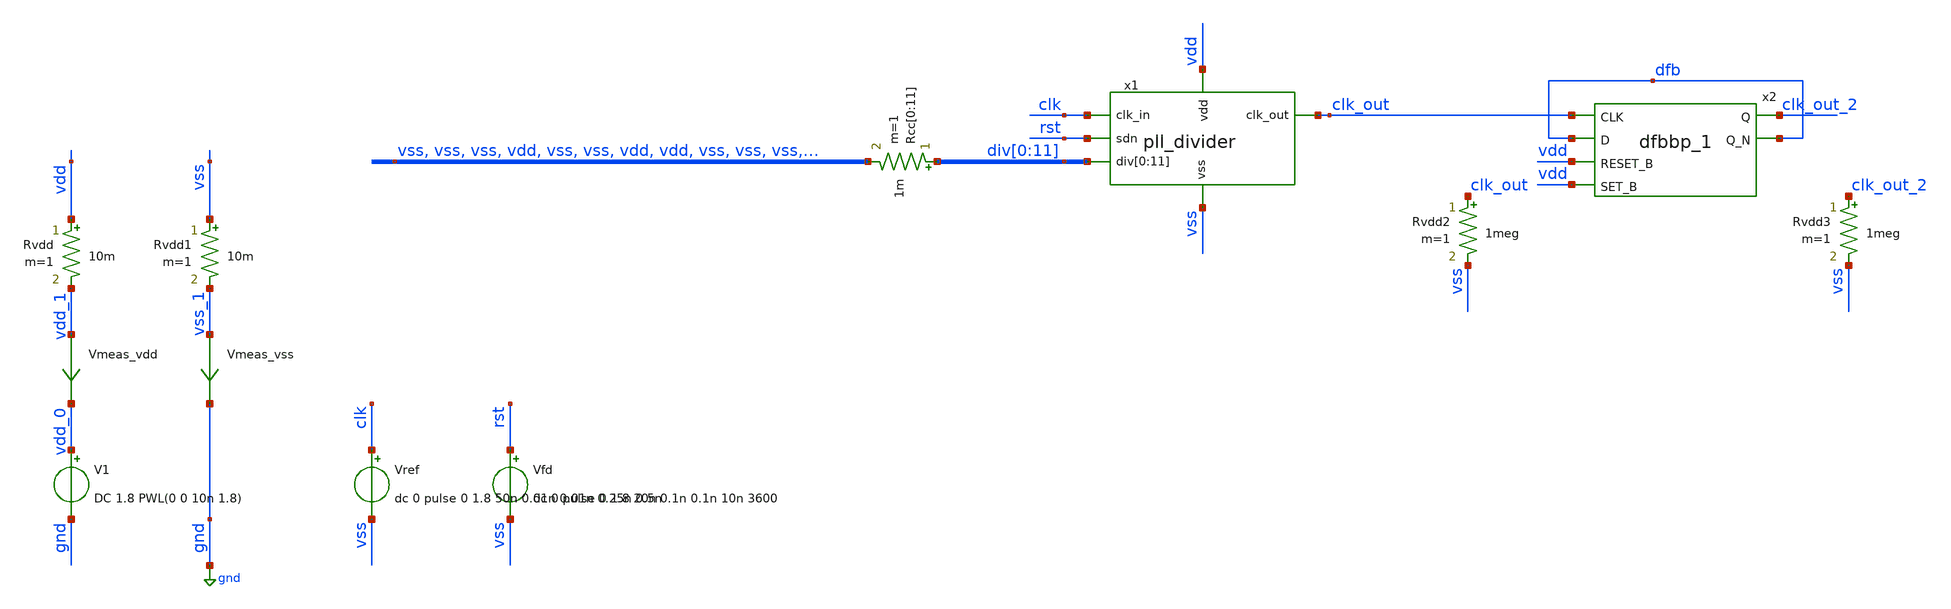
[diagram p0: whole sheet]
** sch_path: pll/pll_divider/simulation/pll_divider_tb.sch
**.subckt pll_divider_tb
V1 vdd_0 gnd DC 1.8 PWL(0 0 10n 1.8)
Vmeas_vdd vdd_1 vdd_0 0
.save i(vmeas_vdd)
Vref clk vss dc 0 pulse 0 1.8 50n 0.01n 0.01n 0.25n 0.5n
Vfd rst vss dc 0 pulse 0 1.8 20n 0.1n 0.1n 10n 3600
Vmeas_vss vss_1 gnd 0
.save i(vmeas_vss)
Rvdd vdd vdd_1 10m m=1
Rvdd1 vss vss_1 10m m=1
Rvdd2 clk_out vss 1meg m=1
Rcc[0] div[0] vss 1m m=1
Rcc[1] div[1] vss 1m m=1
Rcc[2] div[2] vss 1m m=1
Rcc[3] div[3] vdd 1m m=1
Rcc[4] div[4] vss 1m m=1
Rcc[5] div[5] vss 1m m=1
Rcc[6] div[6] vdd 1m m=1
Rcc[7] div[7] vdd 1m m=1
Rcc[8] div[8] vss 1m m=1
Rcc[9] div[9] vss 1m m=1
Rcc[10] div[10] vss 1m m=1
Rcc[11] div[11] vss 1m m=1
Rvdd3 clk_out_2 vss 1meg m=1
x2 clk_out dfb vdd vdd vss vss vdd vdd clk_out_2 dfb sky130_fd_sc_hd__dfbbp_1
x1 vdd vss clk_out clk rst div[0] div[1] div[2] div[3] div[4] div[5] div[6] div[7] div[8] div[9]
+ div[10] div[11] pll_divider
**** begin user architecture code



*.option savecurrents
*.option rshunt = 1e12
*.option gmin = 1e-24

** Settings for PSS osciallator
*.option reltol=1e-5
*.option vntol=3e-8
*.option abstol=1e-13
**.option chgtol=1e-12
*.option trtol=10
.option method=gear

.control

* #################################################################
* #
* #                         OPERATING POINT
* #
* #################################################################
reset
save all

op
set filetype=binary
write pll_divider_tb.raw all

* #################################################################
* #
* #                 TRANSIENT OSCILATION REGIME
* #
* #################################################################
reset
setplot const
*save all
save v(vdd) v(vdd_1) v(vss) v(vss_1)
save v(clk) v(clk_out) v(clk_out_2)
save v(x1.ps_out) v(x1.ps_out_b) v(x1.ps_mod)
save v('x1.q<0>') v('x1.q<1>') v('x1.q<2>') v('x1.q<3>') v('x1.q<4>') v('x1.q<5>') v('x1.q<6>') v('x1.q<7>')
+ v('x1.q<8>') v('x1.q<9>') v('x1.q<10>') v('x1.q<11>')
save v(x1.div_rst) v(x1.int_rst) v(x1.div_rst_b) v(x1.ps_out_b) v(x1.rst_0_2) v(x1.rst_3_11)

tran 0.05n 1u uic
set filetype=ascii
write pll_divider_tb_tran.raw v(clk) v(clk_out)

* Plot outputs
plot v(clk)+2 v(clk_out)+0 v(clk_out_2)-1
plot v(clk)+28 v(x1.ps_out)+26 v(x1.ps_mod)+24 v("x1.q<0>")+22 v("x1.q<1>")+20 v("x1.q<2>")+18
+ v("x1.q<3>")+16 v("x1.q<4>")+14 v("x1.q<5>")+12 v("x1.q<6>")+10 v("x1.q<7>")+8 v("x1.q<8>")+6 v("x1.q<9>")+4
+ v("x1.q<10>")+2 v("x1.q<11>")+0 v(x1.div_rst)-2 v(x1.int_rst)-4  v(x1.div_rst_b)-6 v(x1.rst_0_2)-8
+ v(x1.rst_3_11)-10 v(x1.ps_out_b)-12 v(clk_out)-14

*rusage
.endc



.options wnflag=1
.include $::SKYWATER_MODELS/cells/nfet_01v8/sky130_fd_pr__nfet_01v8__tt.corner.spice
.include $::SKYWATER_MODELS/cells/nfet_01v8_lvt/sky130_fd_pr__nfet_01v8_lvt__tt.corner.spice
.include $::SKYWATER_MODELS/cells/pfet_01v8/sky130_fd_pr__pfet_01v8__tt.corner.spice
.include $::SKYWATER_MODELS/cells/nfet_03v3_nvt/sky130_fd_pr__nfet_03v3_nvt__tt.corner.spice
.include $::SKYWATER_MODELS/cells/nfet_05v0_nvt/sky130_fd_pr__nfet_05v0_nvt__tt.corner.spice
.include $::SKYWATER_MODELS/cells/esd_nfet_01v8/sky130_fd_pr__esd_nfet_01v8__tt.corner.spice
.include $::SKYWATER_MODELS/cells/pfet_01v8_lvt/sky130_fd_pr__pfet_01v8_lvt__tt.corner.spice
.include $::SKYWATER_MODELS/cells/pfet_01v8_hvt/sky130_fd_pr__pfet_01v8_hvt__tt.corner.spice
.include $::SKYWATER_MODELS/cells/esd_pfet_g5v0d10v5/sky130_fd_pr__esd_pfet_g5v0d10v5__tt.corner.spice
.include $::SKYWATER_MODELS/cells/pfet_g5v0d10v5/sky130_fd_pr__pfet_g5v0d10v5__tt.corner.spice
.include $::SKYWATER_MODELS/cells/pfet_g5v0d16v0/sky130_fd_pr__pfet_g5v0d16v0__tt.corner.spice
.include $::SKYWATER_MODELS/cells/nfet_g5v0d10v5/sky130_fd_pr__nfet_g5v0d10v5__tt.corner.spice
.include $::SKYWATER_MODELS/cells/nfet_g5v0d16v0/sky130_fd_pr__nfet_g5v0d16v0__tt_discrete.corner.spice
.include $::SKYWATER_MODELS/cells/esd_nfet_g5v0d10v5/sky130_fd_pr__esd_nfet_g5v0d10v5__tt.corner.spice
.include $::SKYWATER_MODELS/models/corners/tt/nonfet.spice

.include $::SKYWATER_MODELS/cells/cap_var_hvt/sky130_fd_pr__cap_var_hvt.model.spice

* Mismatch parameters
.include $::SKYWATER_MODELS/cells/nfet_01v8/sky130_fd_pr__nfet_01v8__mismatch.corner.spice
.include $::SKYWATER_MODELS/cells/pfet_01v8/sky130_fd_pr__pfet_01v8__mismatch.corner.spice
.include $::SKYWATER_MODELS/cells/nfet_01v8_lvt/sky130_fd_pr__nfet_01v8_lvt__mismatch.corner.spice
.include $::SKYWATER_MODELS/cells/pfet_01v8_lvt/sky130_fd_pr__pfet_01v8_lvt__mismatch.corner.spice
.include $::SKYWATER_MODELS/cells/pfet_01v8_hvt/sky130_fd_pr__pfet_01v8_hvt__mismatch.corner.spice
.include $::SKYWATER_MODELS/cells/nfet_g5v0d10v5/sky130_fd_pr__nfet_g5v0d10v5__mismatch.corner.spice
.include $::SKYWATER_MODELS/cells/pfet_g5v0d10v5/sky130_fd_pr__pfet_g5v0d10v5__mismatch.corner.spice
.include $::SKYWATER_MODELS/cells/nfet_05v0_nvt/sky130_fd_pr__nfet_05v0_nvt__mismatch.corner.spice
.include $::SKYWATER_MODELS/cells/nfet_03v3_nvt/sky130_fd_pr__nfet_03v3_nvt__mismatch.corner.spice

* Resistor$::SKYWATER_MODELS/Capacitor
.include $::SKYWATER_MODELS/models/r+c/res_typical__cap_typical.spice
.include $::SKYWATER_MODELS/models/r+c/res_typical__cap_typical__lin.spice

* Special cells
.include $::SKYWATER_MODELS/models/corners/tt/specialized_cells.spice

* All models
.include $::SKYWATER_MODELS/models/all.spice

* Corner
.include $::SKYWATER_MODELS/models/corners/tt/rf.spice

* .include $::SKYWATER_STDCELLS/cells/
.include $::SKYWATER_STDCELLS/cells/buf/sky130_fd_sc_hd__buf_1.spice
.include $::SKYWATER_STDCELLS_HS/cells/buf/sky130_fd_sc_hs__buf_1.spice
.include $::SKYWATER_STDCELLS_HS/cells/buf/sky130_fd_sc_hs__buf_16.spice
.include $::SKYWATER_STDCELLS/cells/clkbuf/sky130_fd_sc_hd__clkbuf_1.spice
.include $::SKYWATER_STDCELLS/cells/clkbuf/sky130_fd_sc_hd__clkbuf_2.spice
.include $::SKYWATER_STDCELLS/cells/clkbuf/sky130_fd_sc_hd__clkbuf_4.spice
.include $::SKYWATER_STDCELLS/cells/clkbuf/sky130_fd_sc_hd__clkbuf_8.spice
.include $::SKYWATER_STDCELLS/cells/clkbuf/sky130_fd_sc_hd__clkbuf_16.spice
.include $::SKYWATER_STDCELLS/cells/decap/sky130_fd_sc_hd__decap_3.spice
.include $::SKYWATER_STDCELLS/cells/decap/sky130_fd_sc_hd__decap_4.spice
.include $::SKYWATER_STDCELLS/cells/decap/sky130_fd_sc_hd__decap_8.spice
.include $::SKYWATER_STDCELLS/cells/dfrbp/sky130_fd_sc_hd__dfrbp_1.spice
.include $::SKYWATER_STDCELLS/cells/dfrbp/sky130_fd_sc_hd__dfrbp_2.spice
.include $::SKYWATER_STDCELLS/cells/inv/sky130_fd_sc_hd__inv_1.spice
.include $::SKYWATER_STDCELLS/cells/inv/sky130_fd_sc_hd__inv_2.spice
.include $::SKYWATER_STDCELLS/cells/inv/sky130_fd_sc_hd__inv_4.spice
.include $::SKYWATER_STDCELLS/cells/inv/sky130_fd_sc_hd__inv_8.spice
.include $::SKYWATER_STDCELLS/cells/inv/sky130_fd_sc_hd__inv_16.spice
.include $::SKYWATER_STDCELLS_HS/cells/inv/sky130_fd_sc_hs__inv_1.spice
.include $::SKYWATER_STDCELLS_HS/cells/inv/sky130_fd_sc_hs__inv_2.spice
.include $::SKYWATER_STDCELLS_HS/cells/inv/sky130_fd_sc_hs__inv_4.spice
.include $::SKYWATER_STDCELLS_HS/cells/inv/sky130_fd_sc_hs__inv_8.spice
.include $::SKYWATER_STDCELLS_HS/cells/inv/sky130_fd_sc_hs__inv_16.spice
.include $::SKYWATER_STDCELLS/cells/mux2/sky130_fd_sc_hd__mux2_2.spice
.include $::SKYWATER_STDCELLS/cells/nand2/sky130_fd_sc_hd__nand2_1.spice
.include $::SKYWATER_STDCELLS/cells/tap/sky130_fd_sc_hd__tap_2.spice
.include $::SKYWATER_STDCELLS/cells/tapvpwrvgnd/sky130_fd_sc_hd__tapvpwrvgnd_1.spice
.include $::SKYWATER_STDCELLS/cells/dfbbn/sky130_fd_sc_hd__dfbbn_1.spice
.include $::SKYWATER_STDCELLS/cells/dfbbn/sky130_fd_sc_hd__dfbbn_2.spice
.include $::SKYWATER_STDCELLS/cells/dfbbp/sky130_fd_sc_hd__dfbbp_1.spice
.include $::SKYWATER_STDCELLS_HS/cells/dfbbn/sky130_fd_sc_hs__dfbbn_1.spice
.include $::SKYWATER_STDCELLS_HS/cells/dfbbn/sky130_fd_sc_hs__dfbbn_2.spice
.include $::SKYWATER_STDCELLS_HS/cells/dfrbp/sky130_fd_sc_hs__dfrbp_1.spice
.include $::SKYWATER_STDCELLS_HS/cells/dfrbp/sky130_fd_sc_hs__dfrbp_2.spice
.include $::SKYWATER_STDCELLS/cells/dfrtp/sky130_fd_sc_hd__dfrtp_1.spice
.include $::SKYWATER_STDCELLS/cells/dfrtp/sky130_fd_sc_hd__dfrtp_2.spice
.include $::SKYWATER_STDCELLS/cells/dfxbp/sky130_fd_sc_hd__dfxbp_1.spice
.include $::SKYWATER_STDCELLS/cells/dfxbp/sky130_fd_sc_hd__dfxbp_2.spice
.include $::SKYWATER_STDCELLS/cells/or2/sky130_fd_sc_hd__or2_0.spice
.include $::SKYWATER_STDCELLS/cells/or3/sky130_fd_sc_hd__or3_1.spice
.include $::SKYWATER_STDCELLS/cells/nor2/sky130_fd_sc_hd__nor2_1.spice

**** end user architecture code
**.ends

* expanding   symbol:  test_jens/pll/pll_divider/pll_divider.sym # of pins=6
** sym_path: pll/pll_divider/xschem/pll_divider.sym
** sch_path: pll/pll_divider/xschem/pll_divider.sch
.subckt pll_divider vdd vss clk_out clk_in sdn div[0] div[1] div[2] div[3] div[4] div[5] div[6]
+ div[7] div[8] div[9] div[10] div[11]
*.ipin clk_in
*.ipin div[0],div[1],div[2],div[3],div[4],div[5],div[6],div[7],div[8],div[9],div[10],div[11]
*.ipin sdn
*.opin clk_out
*.ipin vss
*.ipin vdd
**** begin user architecture code
* .include $::SKYWATER_STDCELLS/cells/
.include $::SKYWATER_STDCELLS/cells/buf/sky130_fd_sc_hd__buf_1.spice
.include $::SKYWATER_STDCELLS_HS/cells/buf/sky130_fd_sc_hs__buf_1.spice
.include $::SKYWATER_STDCELLS_HS/cells/buf/sky130_fd_sc_hs__buf_16.spice
.include $::SKYWATER_STDCELLS/cells/clkbuf/sky130_fd_sc_hd__clkbuf_1.spice
.include $::SKYWATER_STDCELLS/cells/clkbuf/sky130_fd_sc_hd__clkbuf_2.spice
.include $::SKYWATER_STDCELLS/cells/clkbuf/sky130_fd_sc_hd__clkbuf_4.spice
.include $::SKYWATER_STDCELLS/cells/clkbuf/sky130_fd_sc_hd__clkbuf_8.spice
.include $::SKYWATER_STDCELLS/cells/clkbuf/sky130_fd_sc_hd__clkbuf_16.spice
.include $::SKYWATER_STDCELLS/cells/decap/sky130_fd_sc_hd__decap_3.spice
.include $::SKYWATER_STDCELLS/cells/decap/sky130_fd_sc_hd__decap_4.spice
.include $::SKYWATER_STDCELLS/cells/decap/sky130_fd_sc_hd__decap_8.spice
.include $::SKYWATER_STDCELLS/cells/dfrbp/sky130_fd_sc_hd__dfrbp_1.spice
.include $::SKYWATER_STDCELLS/cells/dfrbp/sky130_fd_sc_hd__dfrbp_2.spice
.include $::SKYWATER_STDCELLS/cells/inv/sky130_fd_sc_hd__inv_1.spice
.include $::SKYWATER_STDCELLS/cells/inv/sky130_fd_sc_hd__inv_2.spice
.include $::SKYWATER_STDCELLS/cells/inv/sky130_fd_sc_hd__inv_4.spice
.include $::SKYWATER_STDCELLS/cells/inv/sky130_fd_sc_hd__inv_8.spice
.include $::SKYWATER_STDCELLS/cells/inv/sky130_fd_sc_hd__inv_16.spice
.include $::SKYWATER_STDCELLS_HS/cells/inv/sky130_fd_sc_hs__inv_1.spice
.include $::SKYWATER_STDCELLS_HS/cells/inv/sky130_fd_sc_hs__inv_2.spice
.include $::SKYWATER_STDCELLS_HS/cells/inv/sky130_fd_sc_hs__inv_4.spice
.include $::SKYWATER_STDCELLS_HS/cells/inv/sky130_fd_sc_hs__inv_8.spice
.include $::SKYWATER_STDCELLS_HS/cells/inv/sky130_fd_sc_hs__inv_16.spice
.include $::SKYWATER_STDCELLS/cells/mux2/sky130_fd_sc_hd__mux2_2.spice
.include $::SKYWATER_STDCELLS/cells/and2/sky130_fd_sc_hd__and2_1.spice
.include $::SKYWATER_STDCELLS/cells/and2/sky130_fd_sc_hd__and2_2.spice
.include $::SKYWATER_STDCELLS/cells/nand2/sky130_fd_sc_hd__nand2_1.spice
.include $::SKYWATER_STDCELLS/cells/tap/sky130_fd_sc_hd__tap_2.spice
.include $::SKYWATER_STDCELLS/cells/tapvpwrvgnd/sky130_fd_sc_hd__tapvpwrvgnd_1.spice
.include $::SKYWATER_STDCELLS/cells/dfbbn/sky130_fd_sc_hd__dfbbn_1.spice
.include $::SKYWATER_STDCELLS/cells/dfbbn/sky130_fd_sc_hd__dfbbn_2.spice
.include $::SKYWATER_STDCELLS/cells/dfbbp/sky130_fd_sc_hd__dfbbp_1.spice
.include $::SKYWATER_STDCELLS_HS/cells/dfbbn/sky130_fd_sc_hs__dfbbn_1.spice
.include $::SKYWATER_STDCELLS_HS/cells/dfbbn/sky130_fd_sc_hs__dfbbn_2.spice
.include $::SKYWATER_STDCELLS_HS/cells/dfrbp/sky130_fd_sc_hs__dfrbp_1.spice
.include $::SKYWATER_STDCELLS_HS/cells/dfrbp/sky130_fd_sc_hs__dfrbp_2.spice
.include $::SKYWATER_STDCELLS/cells/dfrtp/sky130_fd_sc_hd__dfrtp_1.spice
.include $::SKYWATER_STDCELLS/cells/dfrtp/sky130_fd_sc_hd__dfrtp_2.spice
.include $::SKYWATER_STDCELLS/cells/dfxbp/sky130_fd_sc_hd__dfxbp_1.spice
.include $::SKYWATER_STDCELLS/cells/dfxbp/sky130_fd_sc_hd__dfxbp_2.spice
.include $::SKYWATER_STDCELLS/cells/or2/sky130_fd_sc_hd__or2_0.spice
.include $::SKYWATER_STDCELLS/cells/or3/sky130_fd_sc_hd__or3_1.spice
.include $::SKYWATER_STDCELLS/cells/nor2/sky130_fd_sc_hd__nor2_1.spice
.include $::SKYWATER_STDCELLS/cells/nor3/sky130_fd_sc_hd__nor3_1.spice

**** end user architecture code
x1 clk_in net4 vdd vss vss vdd vdd net1 net63 sky130_fd_sc_hd__dfrbp_1
x2 clk_in net1 vdd vss vss vdd vdd net2 net64 sky130_fd_sc_hd__dfrbp_1
x4 clk_in net3 vdd vss vss vdd vdd net5 net65 sky130_fd_sc_hd__dfrbp_1
x5 net1 net6 vdd vss vss vdd vdd ps_out net6 sky130_fd_sc_hd__dfrbp_1
x3 ps_out net2 ps_mod vss vss vdd vdd net3 sky130_fd_sc_hd__or3_1
x6 net2 net5 vss vss vdd vdd net4 sky130_fd_sc_hd__nand2_1
x7 net52 net9 net7 net8 vss vss vdd vdd Q[0] net9 sky130_fd_sc_hd__dfbbp_1
x8 Q[0] net12 net10 net11 vss vss vdd vdd Q[1] net12 sky130_fd_sc_hd__dfbbp_1
x9 Q[1] net15 net13 net14 vss vss vdd vdd Q[2] net15 sky130_fd_sc_hd__dfbbp_1
x10 ps_out QN rs ss vss vss vdd vdd Q[3] QN sky130_fd_sc_hd__dfbbp_1
x11 Q[3] net18 net16 net17 vss vss vdd vdd Q[4] net18 sky130_fd_sc_hd__dfbbp_1
x12 Q[4] net21 net19 net20 vss vss vdd vdd Q[5] net21 sky130_fd_sc_hd__dfbbp_1
x13 Q[5] net24 net22 net23 vss vss vdd vdd Q[6] net24 sky130_fd_sc_hd__dfbbp_1
x14 Q[6] net27 net25 net26 vss vss vdd vdd Q[7] net27 sky130_fd_sc_hd__dfbbp_1
x15 Q[7] net30 net28 net29 vss vss vdd vdd Q[8] net30 sky130_fd_sc_hd__dfbbp_1
x16 Q[8] net33 net31 net32 vss vss vdd vdd Q[9] net33 sky130_fd_sc_hd__dfbbp_1
x17 Q[9] net36 net34 net35 vss vss vdd vdd Q[10] net36 sky130_fd_sc_hd__dfbbp_1
x18 Q[10] net39 net37 net38 vss vss vdd vdd Q[11] net39 sky130_fd_sc_hd__dfbbp_1
x19 rst_0_2 net40 vss vss vdd vdd net7 sky130_fd_sc_hd__nand2_1
x20 rst_0_2 div[0] vss vss vdd vdd net8 sky130_fd_sc_hd__nand2_1
x21 div[0] vss vss vdd vdd net40 sky130_fd_sc_hd__inv_1
x22 rst_0_2 net41 vss vss vdd vdd net10 sky130_fd_sc_hd__nand2_1
x23 rst_0_2 div[1] vss vss vdd vdd net11 sky130_fd_sc_hd__nand2_1
x24 div[1] vss vss vdd vdd net41 sky130_fd_sc_hd__inv_1
x25 rst_0_2 net42 vss vss vdd vdd net13 sky130_fd_sc_hd__nand2_1
x26 rst_0_2 div[2] vss vss vdd vdd net14 sky130_fd_sc_hd__nand2_1
x27 div[2] vss vss vdd vdd net42 sky130_fd_sc_hd__inv_1
x28 rst_3_11 net43 vss vss vdd vdd rs sky130_fd_sc_hd__nand2_1
x29 rst_3_11 div[3] vss vss vdd vdd ss sky130_fd_sc_hd__nand2_1
x30 div[3] vss vss vdd vdd net43 sky130_fd_sc_hd__inv_1
x31 rst_3_11 net44 vss vss vdd vdd net16 sky130_fd_sc_hd__nand2_1
x32 rst_3_11 div[4] vss vss vdd vdd net17 sky130_fd_sc_hd__nand2_1
x33 div[4] vss vss vdd vdd net44 sky130_fd_sc_hd__inv_1
x34 rst_3_11 net45 vss vss vdd vdd net19 sky130_fd_sc_hd__nand2_1
x35 rst_3_11 div[5] vss vss vdd vdd net20 sky130_fd_sc_hd__nand2_1
x36 div[5] vss vss vdd vdd net45 sky130_fd_sc_hd__inv_1
x37 rst_3_11 net46 vss vss vdd vdd net22 sky130_fd_sc_hd__nand2_1
x38 rst_3_11 div[6] vss vss vdd vdd net23 sky130_fd_sc_hd__nand2_1
x39 div[6] vss vss vdd vdd net46 sky130_fd_sc_hd__inv_1
x40 rst_3_11 net47 vss vss vdd vdd net25 sky130_fd_sc_hd__nand2_1
x41 rst_3_11 div[7] vss vss vdd vdd net26 sky130_fd_sc_hd__nand2_1
x42 div[7] vss vss vdd vdd net47 sky130_fd_sc_hd__inv_1
x43 rst_3_11 net48 vss vss vdd vdd net28 sky130_fd_sc_hd__nand2_1
x44 rst_3_11 div[8] vss vss vdd vdd net29 sky130_fd_sc_hd__nand2_1
x45 div[8] vss vss vdd vdd net48 sky130_fd_sc_hd__inv_1
x46 rst_3_11 net49 vss vss vdd vdd net31 sky130_fd_sc_hd__nand2_1
x47 rst_3_11 div[9] vss vss vdd vdd net32 sky130_fd_sc_hd__nand2_1
x48 div[9] vss vss vdd vdd net49 sky130_fd_sc_hd__inv_1
x49 rst_3_11 net50 vss vss vdd vdd net34 sky130_fd_sc_hd__nand2_1
x50 rst_3_11 div[10] vss vss vdd vdd net35 sky130_fd_sc_hd__nand2_1
x51 div[10] vss vss vdd vdd net50 sky130_fd_sc_hd__inv_1
x52 rst_3_11 net51 vss vss vdd vdd net37 sky130_fd_sc_hd__nand2_1
x53 rst_3_11 div[11] vss vss vdd vdd net38 sky130_fd_sc_hd__nand2_1
x54 div[11] vss vss vdd vdd net51 sky130_fd_sc_hd__inv_1
x55 Q[2] Q[1] vss vss vdd vdd net53 sky130_fd_sc_hd__or2_0
x56 net53 Q[0] vss vss vdd vdd ps_mod sky130_fd_sc_hd__nor2_1
x58 ps_mod vss vss vdd vdd net54 sky130_fd_sc_hd__inv_1
x59 Q[11] Q[10] vss vss vdd vdd net58 sky130_fd_sc_hd__or2_0
x60 net58 Q[9] vss vss vdd vdd net60 sky130_fd_sc_hd__or2_0
x61 net60 Q[8] vss vss vdd vdd net61 sky130_fd_sc_hd__or2_0
x62 net61 Q[7] vss vss vdd vdd net62 sky130_fd_sc_hd__or2_0
x63 net62 Q[6] vss vss vdd vdd net57 sky130_fd_sc_hd__or2_0
x64 net57 Q[5] vss vss vdd vdd net56 sky130_fd_sc_hd__or2_0
x65 net56 Q[4] vss vss vdd vdd net55 sky130_fd_sc_hd__or2_0
x66 net55 Q[3] vss vss vdd vdd div_rst sky130_fd_sc_hd__nor2_1
x67 int_rst sdn div_rst vss vss vdd vdd div_rst_b sky130_fd_sc_hd__nor3_1
x68 div_rst_b vss vss vdd vdd rst_3_11 sky130_fd_sc_hd__inv_2
x69 div_rst_b vss vss vdd vdd rst_0_2 sky130_fd_sc_hd__inv_2
x70 div_rst vdd net59 vss vss vdd vdd int_rst sky130_fd_sc_hd__dfrtp_1
x71 int_rst ps_out_b vss vss vdd vdd net59 sky130_fd_sc_hd__nand2_1
x73 ps_out_b div_rst_b vss vss vdd vdd net66 clk_out sky130_fd_sc_hd__dfxbp_1
x72 ps_out vss vss vdd vdd ps_out_b sky130_fd_sc_hd__inv_2
x57 net54 ps_out vss vss vdd vdd net52 sky130_fd_sc_hd__and2_2
* noconn vss
* noconn vdd
* noconn #net65
* noconn #net64
* noconn #net63
* noconn #net66
.ends

.GLOBAL gnd
.end
